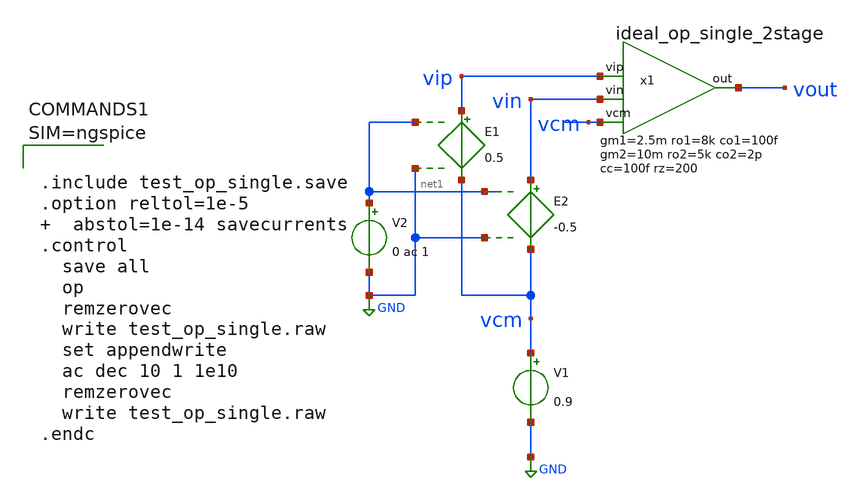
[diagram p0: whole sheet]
** sch_path: test_op_single.sch
**.subckt test_op_single
E1 vip vcm net1 GND 0.5
E2 vin vcm net1 GND -0.5
V1 vcm GND 0.9
V2 net1 GND 0 ac 1
x1 vout vip vin vcm ideal_op_single_2stage gm1=2.5m ro1=8k co1=100f gm2=10m ro2=5k co2=2p cc=100f
+ rz=200
**** begin user architecture code



.include test_op_single.save
.option reltol=1e-5   abstol=1e-14 savecurrents
.control
  save all
  op
  remzerovec
  write test_op_single.raw
  set appendwrite
  ac dec 10 1 1e10
  remzerovec
  write test_op_single.raw
.endc



**** end user architecture code
**.ends

* expanding   symbol:  /home/tester/proj/modules/ideal_op_single_2stage.sym # of pins=4
** sym_path: modules/ideal_op_single_2stage.sym
** sch_path: modules/ideal_op_single_2stage.sch
.subckt ideal_op_single_2stage out vip vin vcm  gm1=5m ro1=20k co1=100f gm2=10m ro2=5k co2=2p
+ cc=100f rz=200
*.ipin vip
*.ipin vin
*.opin out
*.ipin vcm
G1 net1 vcm vip vin {gm1}
R1 net1 vcm {ro1} m=1
C1 net1 vcm {co1} m=1
G3 out vcm net1 vcm {gm2}
R3 out vcm {ro2} m=1
C3 out vcm {co2} m=1
R5 net1 net2 {rz} m=1
C5 net2 out {cc} m=1
.ends

.GLOBAL GND
.end
